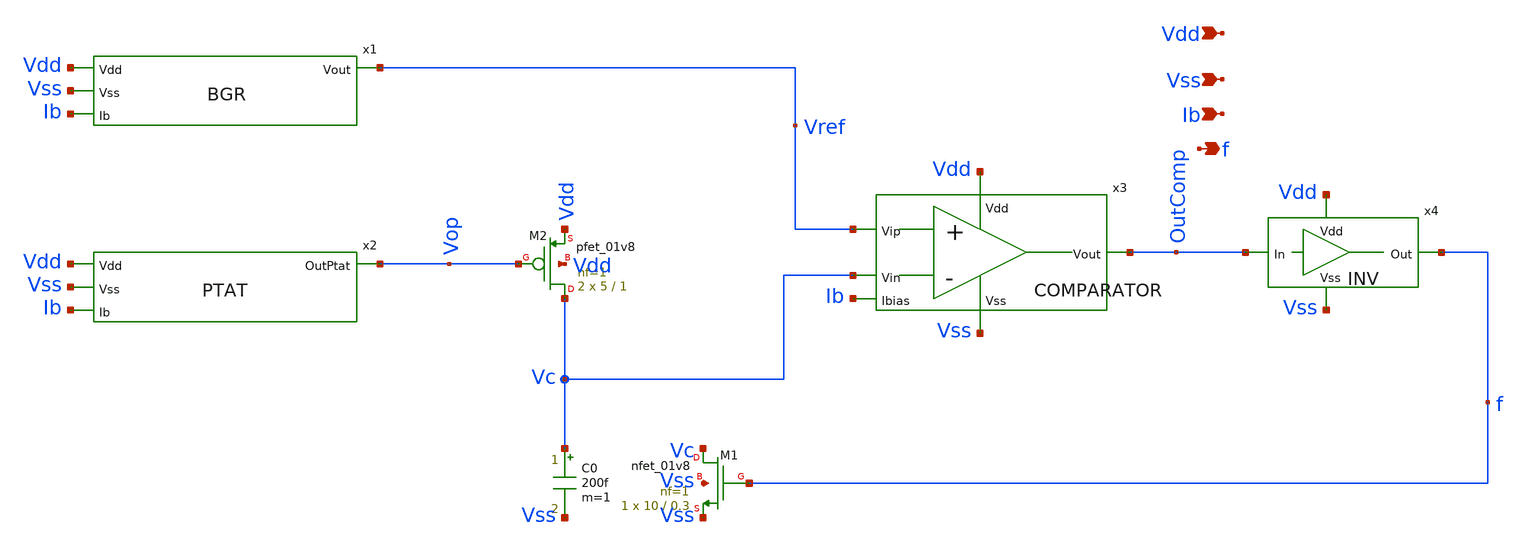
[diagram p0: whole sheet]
** sch_path: temp_sensor_sky130nm/design/TEMP_SENSOR_SKY130NM/TEMP_SENSOR.sch
**.subckt TEMP_SENSOR Vdd Vss Ib f
*.ipin Vdd
*.ipin Vss
*.ipin Ib
*.opin f
XM2 Vc Vop Vdd Vdd sky130_fd_pr__pfet_01v8 L=1 W=5 nf=1 ad='int((nf+1)/2) * W/nf * 0.29' as='int((nf+2)/2) * W/nf * 0.29'
+ pd='2*int((nf+1)/2) * (W/nf + 0.29)' ps='2*int((nf+2)/2) * (W/nf + 0.29)' nrd='0.29 / W' nrs='0.29 / W'
+ sa=0 sb=0 sd=0 mult=2 m=2
C0 Vc Vss 200f m=1
XM1 Vc f Vss Vss sky130_fd_pr__nfet_01v8 L=0.3 W=10 nf=1 ad='int((nf+1)/2) * W/nf * 0.29' as='int((nf+2)/2) * W/nf * 0.29'
+ pd='2*int((nf+1)/2) * (W/nf + 0.29)' ps='2*int((nf+2)/2) * (W/nf + 0.29)' nrd='0.29 / W' nrs='0.29 / W'
+ sa=0 sb=0 sd=0 mult=1 m=1
x1 Vdd Vss Ib Vref BGR
x2 Vdd Vss Ib Vop PTAT
x3 Vdd Vss Vref Vc Ib OutComp COMPARATOR
x4 Vdd Vss OutComp f INV
**.ends

* expanding   symbol:  TEMP_SENSOR_SKY130NM/BGR.sym # of pins=4
** sym_path: temp_sensor_sky130nm/design/TEMP_SENSOR_SKY130NM/BGR.sym
** sch_path: temp_sensor_sky130nm/design/TEMP_SENSOR_SKY130NM/BGR.sch
.subckt BGR Vdd Vss Ib Vout
*.ipin Vdd
*.ipin Vss
*.ipin Ib
*.opin Vout
XM1 B A Vdd Vdd sky130_fd_pr__pfet_01v8 L=1 W=5 nf=1 ad='int((nf+1)/2) * W/nf * 0.29' as='int((nf+2)/2) * W/nf * 0.29'
+ pd='2*int((nf+1)/2) * (W/nf + 0.29)' ps='2*int((nf+2)/2) * (W/nf + 0.29)' nrd='0.29 / W' nrs='0.29 / W'
+ sa=0 sb=0 sd=0 mult=2 m=2
XM2 C A Vdd Vdd sky130_fd_pr__pfet_01v8 L=1 W=5 nf=1 ad='int((nf+1)/2) * W/nf * 0.29' as='int((nf+2)/2) * W/nf * 0.29'
+ pd='2*int((nf+1)/2) * (W/nf + 0.29)' ps='2*int((nf+2)/2) * (W/nf + 0.29)' nrd='0.29 / W' nrs='0.29 / W'
+ sa=0 sb=0 sd=0 mult=2 m=2
XQ1 Vss Vss B sky130_fd_pr__pnp_05v5_W3p40L3p40 m=1
XQ2 Vss Vss net1 sky130_fd_pr__pnp_05v5_W3p40L3p40 m=8
XQ3 Vss Vss net2 sky130_fd_pr__pnp_05v5_W3p40L3p40 m=1
XM3 Vout A Vdd Vdd sky130_fd_pr__pfet_01v8 L=1 W=5 nf=1 ad='int((nf+1)/2) * W/nf * 0.29' as='int((nf+2)/2) * W/nf * 0.29'
+ pd='2*int((nf+1)/2) * (W/nf + 0.29)' ps='2*int((nf+2)/2) * (W/nf + 0.29)' nrd='0.29 / W' nrs='0.29 / W'
+ sa=0 sb=0 sd=0 mult=2 m=2
R1 C net1 5.3k m=1
R2 Vout net2 48k m=1
x1 Vdd Vss C B Ib A OTA
.ends


* expanding   symbol:  TEMP_SENSOR_SKY130NM/PTAT.sym # of pins=4
** sym_path: temp_sensor_sky130nm/design/TEMP_SENSOR_SKY130NM/PTAT.sym
** sch_path: temp_sensor_sky130nm/design/TEMP_SENSOR_SKY130NM/PTAT.sch
.subckt PTAT Vdd Vss Ib OutPtat
*.ipin Vdd
*.ipin Vss
*.ipin Ib
*.opin OutPtat
XM1 B OutPtat Vdd Vdd sky130_fd_pr__pfet_01v8 L=1 W=5 nf=1 ad='int((nf+1)/2) * W/nf * 0.29' as='int((nf+2)/2) * W/nf * 0.29'
+ pd='2*int((nf+1)/2) * (W/nf + 0.29)' ps='2*int((nf+2)/2) * (W/nf + 0.29)' nrd='0.29 / W' nrs='0.29 / W'
+ sa=0 sb=0 sd=0 mult=2 m=2
XM2 C OutPtat Vdd Vdd sky130_fd_pr__pfet_01v8 L=1 W=5 nf=1 ad='int((nf+1)/2) * W/nf * 0.29' as='int((nf+2)/2) * W/nf * 0.29'
+ pd='2*int((nf+1)/2) * (W/nf + 0.29)' ps='2*int((nf+2)/2) * (W/nf + 0.29)' nrd='0.29 / W' nrs='0.29 / W'
+ sa=0 sb=0 sd=0 mult=2 m=2
XQ1 Vss Vss B sky130_fd_pr__pnp_05v5_W3p40L3p40 m=1
XQ2 Vss Vss net1 sky130_fd_pr__pnp_05v5_W3p40L3p40 m=8
R1 C net1 5.3k m=1
x1 Vdd Vss C B Ib OutPtat OTA
.ends


* expanding   symbol:  TEMP_SENSOR_SKY130NM/COMPARATOR.sym # of pins=6
** sym_path: temp_sensor_sky130nm/design/TEMP_SENSOR_SKY130NM/COMPARATOR.sym
** sch_path: temp_sensor_sky130nm/design/TEMP_SENSOR_SKY130NM/COMPARATOR.sch
.subckt COMPARATOR Vdd Vss Vip Vin Ibias Vout
*.ipin Vdd
*.ipin Vss
*.ipin Vip
*.ipin Vin
*.ipin Ibias
*.opin Vout
XM1 net1 net1 Vdd Vdd sky130_fd_pr__pfet_01v8 L=1 W=1 nf=1 ad='int((nf+1)/2) * W/nf * 0.29' as='int((nf+2)/2) * W/nf * 0.29'
+ pd='2*int((nf+1)/2) * (W/nf + 0.29)' ps='2*int((nf+2)/2) * (W/nf + 0.29)' nrd='0.29 / W' nrs='0.29 / W'
+ sa=0 sb=0 sd=0 mult=1 m=1
XM2 Vo1 net1 Vdd Vdd sky130_fd_pr__pfet_01v8 L=1 W=1 nf=1 ad='int((nf+1)/2) * W/nf * 0.29' as='int((nf+2)/2) * W/nf * 0.29'
+ pd='2*int((nf+1)/2) * (W/nf + 0.29)' ps='2*int((nf+2)/2) * (W/nf + 0.29)' nrd='0.29 / W' nrs='0.29 / W'
+ sa=0 sb=0 sd=0 mult=1 m=1
XM3 net1 Vip net2 Vss sky130_fd_pr__nfet_01v8 L=1 W=1 nf=1 ad='int((nf+1)/2) * W/nf * 0.29' as='int((nf+2)/2) * W/nf * 0.29'
+ pd='2*int((nf+1)/2) * (W/nf + 0.29)' ps='2*int((nf+2)/2) * (W/nf + 0.29)' nrd='0.29 / W' nrs='0.29 / W'
+ sa=0 sb=0 sd=0 mult=1 m=1
XM4 Vo1 Vin net2 Vss sky130_fd_pr__nfet_01v8 L=1 W=1 nf=1 ad='int((nf+1)/2) * W/nf * 0.29' as='int((nf+2)/2) * W/nf * 0.29'
+ pd='2*int((nf+1)/2) * (W/nf + 0.29)' ps='2*int((nf+2)/2) * (W/nf + 0.29)' nrd='0.29 / W' nrs='0.29 / W'
+ sa=0 sb=0 sd=0 mult=1 m=1
XM9 net2 Ibias Vss Vss sky130_fd_pr__nfet_01v8 L=1 W=1 nf=1 ad='int((nf+1)/2) * W/nf * 0.29' as='int((nf+2)/2) * W/nf * 0.29'
+ pd='2*int((nf+1)/2) * (W/nf + 0.29)' ps='2*int((nf+2)/2) * (W/nf + 0.29)' nrd='0.29 / W' nrs='0.29 / W'
+ sa=0 sb=0 sd=0 mult=1 m=1
XM8 Vo2 Vo1 Vdd Vdd sky130_fd_pr__pfet_01v8 L=1 W=6 nf=1 ad='int((nf+1)/2) * W/nf * 0.29' as='int((nf+2)/2) * W/nf * 0.29'
+ pd='2*int((nf+1)/2) * (W/nf + 0.29)' ps='2*int((nf+2)/2) * (W/nf + 0.29)' nrd='0.29 / W' nrs='0.29 / W'
+ sa=0 sb=0 sd=0 mult=1 m=1
XM10 Vo2 Ibias Vss Vss sky130_fd_pr__nfet_01v8 L=1 W=1 nf=1 ad='int((nf+1)/2) * W/nf * 0.29' as='int((nf+2)/2) * W/nf * 0.29'
+ pd='2*int((nf+1)/2) * (W/nf + 0.29)' ps='2*int((nf+2)/2) * (W/nf + 0.29)' nrd='0.29 / W' nrs='0.29 / W'
+ sa=0 sb=0 sd=0 mult=1 m=1
XM11 Vout Vo2 Vdd Vdd sky130_fd_pr__pfet_01v8 L=1 W=3 nf=1 ad='int((nf+1)/2) * W/nf * 0.29' as='int((nf+2)/2) * W/nf * 0.29'
+ pd='2*int((nf+1)/2) * (W/nf + 0.29)' ps='2*int((nf+2)/2) * (W/nf + 0.29)' nrd='0.29 / W' nrs='0.29 / W'
+ sa=0 sb=0 sd=0 mult=1 m=1
XM13 Vout Vo2 Vss Vss sky130_fd_pr__nfet_01v8 L=1 W=1 nf=1 ad='int((nf+1)/2) * W/nf * 0.29' as='int((nf+2)/2) * W/nf * 0.29'
+ pd='2*int((nf+1)/2) * (W/nf + 0.29)' ps='2*int((nf+2)/2) * (W/nf + 0.29)' nrd='0.29 / W' nrs='0.29 / W'
+ sa=0 sb=0 sd=0 mult=1 m=1
XM12 Ibias Ibias Vss Vss sky130_fd_pr__nfet_01v8 L=1 W=1 nf=1 ad='int((nf+1)/2) * W/nf * 0.29' as='int((nf+2)/2) * W/nf * 0.29'
+ pd='2*int((nf+1)/2) * (W/nf + 0.29)' ps='2*int((nf+2)/2) * (W/nf + 0.29)' nrd='0.29 / W' nrs='0.29 / W'
+ sa=0 sb=0 sd=0 mult=1 m=1
.ends


* expanding   symbol:  TEMP_SENSOR_SKY130NM/INV.sym # of pins=4
** sym_path: temp_sensor_sky130nm/design/TEMP_SENSOR_SKY130NM/INV.sym
** sch_path: temp_sensor_sky130nm/design/TEMP_SENSOR_SKY130NM/INV.sch
.subckt INV Vdd Vss In Out
*.ipin Vdd
*.ipin Vss
*.ipin In
*.opin Out
XM7 Out In Vdd Vdd sky130_fd_pr__pfet_01v8 L=0.5 W=3 nf=1 ad='int((nf+1)/2) * W/nf * 0.29' as='int((nf+2)/2) * W/nf * 0.29'
+ pd='2*int((nf+1)/2) * (W/nf + 0.29)' ps='2*int((nf+2)/2) * (W/nf + 0.29)' nrd='0.29 / W' nrs='0.29 / W'
+ sa=0 sb=0 sd=0 mult=1 m=1
XM8 Out In Vss Vss sky130_fd_pr__nfet_01v8 L=0.5 W=1 nf=1 ad='int((nf+1)/2) * W/nf * 0.29' as='int((nf+2)/2) * W/nf * 0.29'
+ pd='2*int((nf+1)/2) * (W/nf + 0.29)' ps='2*int((nf+2)/2) * (W/nf + 0.29)' nrd='0.29 / W' nrs='0.29 / W'
+ sa=0 sb=0 sd=0 mult=1 m=1
.ends


* expanding   symbol:  TEMP_SENSOR_SKY130NM/OTA.sym # of pins=6
** sym_path: temp_sensor_sky130nm/design/TEMP_SENSOR_SKY130NM/OTA.sym
** sch_path: temp_sensor_sky130nm/design/TEMP_SENSOR_SKY130NM/OTA.sch
.subckt OTA Vdd Vss Vip Vin Ib Vout
*.ipin Vdd
*.ipin Vss
*.ipin Vip
*.ipin Vin
*.ipin Ib
*.opin Vout
Cc Vout net3 800f m=1
XM1 net2 Vin net1 net1 sky130_fd_pr__pfet_01v8 L=1 W=3 nf=1 ad='int((nf+1)/2) * W/nf * 0.29' as='int((nf+2)/2) * W/nf * 0.29'
+ pd='2*int((nf+1)/2) * (W/nf + 0.29)' ps='2*int((nf+2)/2) * (W/nf + 0.29)' nrd='0.29 / W' nrs='0.29 / W'
+ sa=0 sb=0 sd=0 mult=1 m=1
XM2 net3 Vip net1 net1 sky130_fd_pr__pfet_01v8 L=1 W=3 nf=1 ad='int((nf+1)/2) * W/nf * 0.29' as='int((nf+2)/2) * W/nf * 0.29'
+ pd='2*int((nf+1)/2) * (W/nf + 0.29)' ps='2*int((nf+2)/2) * (W/nf + 0.29)' nrd='0.29 / W' nrs='0.29 / W'
+ sa=0 sb=0 sd=0 mult=1 m=1
XM3 net2 net2 Vss Vss sky130_fd_pr__nfet_01v8 L=1 W=1 nf=1 ad='int((nf+1)/2) * W/nf * 0.29' as='int((nf+2)/2) * W/nf * 0.29'
+ pd='2*int((nf+1)/2) * (W/nf + 0.29)' ps='2*int((nf+2)/2) * (W/nf + 0.29)' nrd='0.29 / W' nrs='0.29 / W'
+ sa=0 sb=0 sd=0 mult=1 m=1
XM4 net3 net2 Vss Vss sky130_fd_pr__nfet_01v8 L=1 W=1 nf=1 ad='int((nf+1)/2) * W/nf * 0.29' as='int((nf+2)/2) * W/nf * 0.29'
+ pd='2*int((nf+1)/2) * (W/nf + 0.29)' ps='2*int((nf+2)/2) * (W/nf + 0.29)' nrd='0.29 / W' nrs='0.29 / W'
+ sa=0 sb=0 sd=0 mult=1 m=1
XM5 net1 Ib Vdd Vdd sky130_fd_pr__pfet_01v8 L=1 W=6 nf=1 ad='int((nf+1)/2) * W/nf * 0.29' as='int((nf+2)/2) * W/nf * 0.29'
+ pd='2*int((nf+1)/2) * (W/nf + 0.29)' ps='2*int((nf+2)/2) * (W/nf + 0.29)' nrd='0.29 / W' nrs='0.29 / W'
+ sa=0 sb=0 sd=0 mult=1 m=1
XM6 Vout Ib Vdd Vdd sky130_fd_pr__pfet_01v8 L=1 W=6 nf=1 ad='int((nf+1)/2) * W/nf * 0.29' as='int((nf+2)/2) * W/nf * 0.29'
+ pd='2*int((nf+1)/2) * (W/nf + 0.29)' ps='2*int((nf+2)/2) * (W/nf + 0.29)' nrd='0.29 / W' nrs='0.29 / W'
+ sa=0 sb=0 sd=0 mult=1 m=1
XM7 Vout net3 Vss Vss sky130_fd_pr__nfet_01v8 L=1 W=2 nf=1 ad='int((nf+1)/2) * W/nf * 0.29' as='int((nf+2)/2) * W/nf * 0.29'
+ pd='2*int((nf+1)/2) * (W/nf + 0.29)' ps='2*int((nf+2)/2) * (W/nf + 0.29)' nrd='0.29 / W' nrs='0.29 / W'
+ sa=0 sb=0 sd=0 mult=1 m=1
XM8 Ib Ib Vdd Vdd sky130_fd_pr__pfet_01v8 L=1 W=6 nf=1 ad='int((nf+1)/2) * W/nf * 0.29' as='int((nf+2)/2) * W/nf * 0.29'
+ pd='2*int((nf+1)/2) * (W/nf + 0.29)' ps='2*int((nf+2)/2) * (W/nf + 0.29)' nrd='0.29 / W' nrs='0.29 / W'
+ sa=0 sb=0 sd=0 mult=1 m=1
.ends

.end
